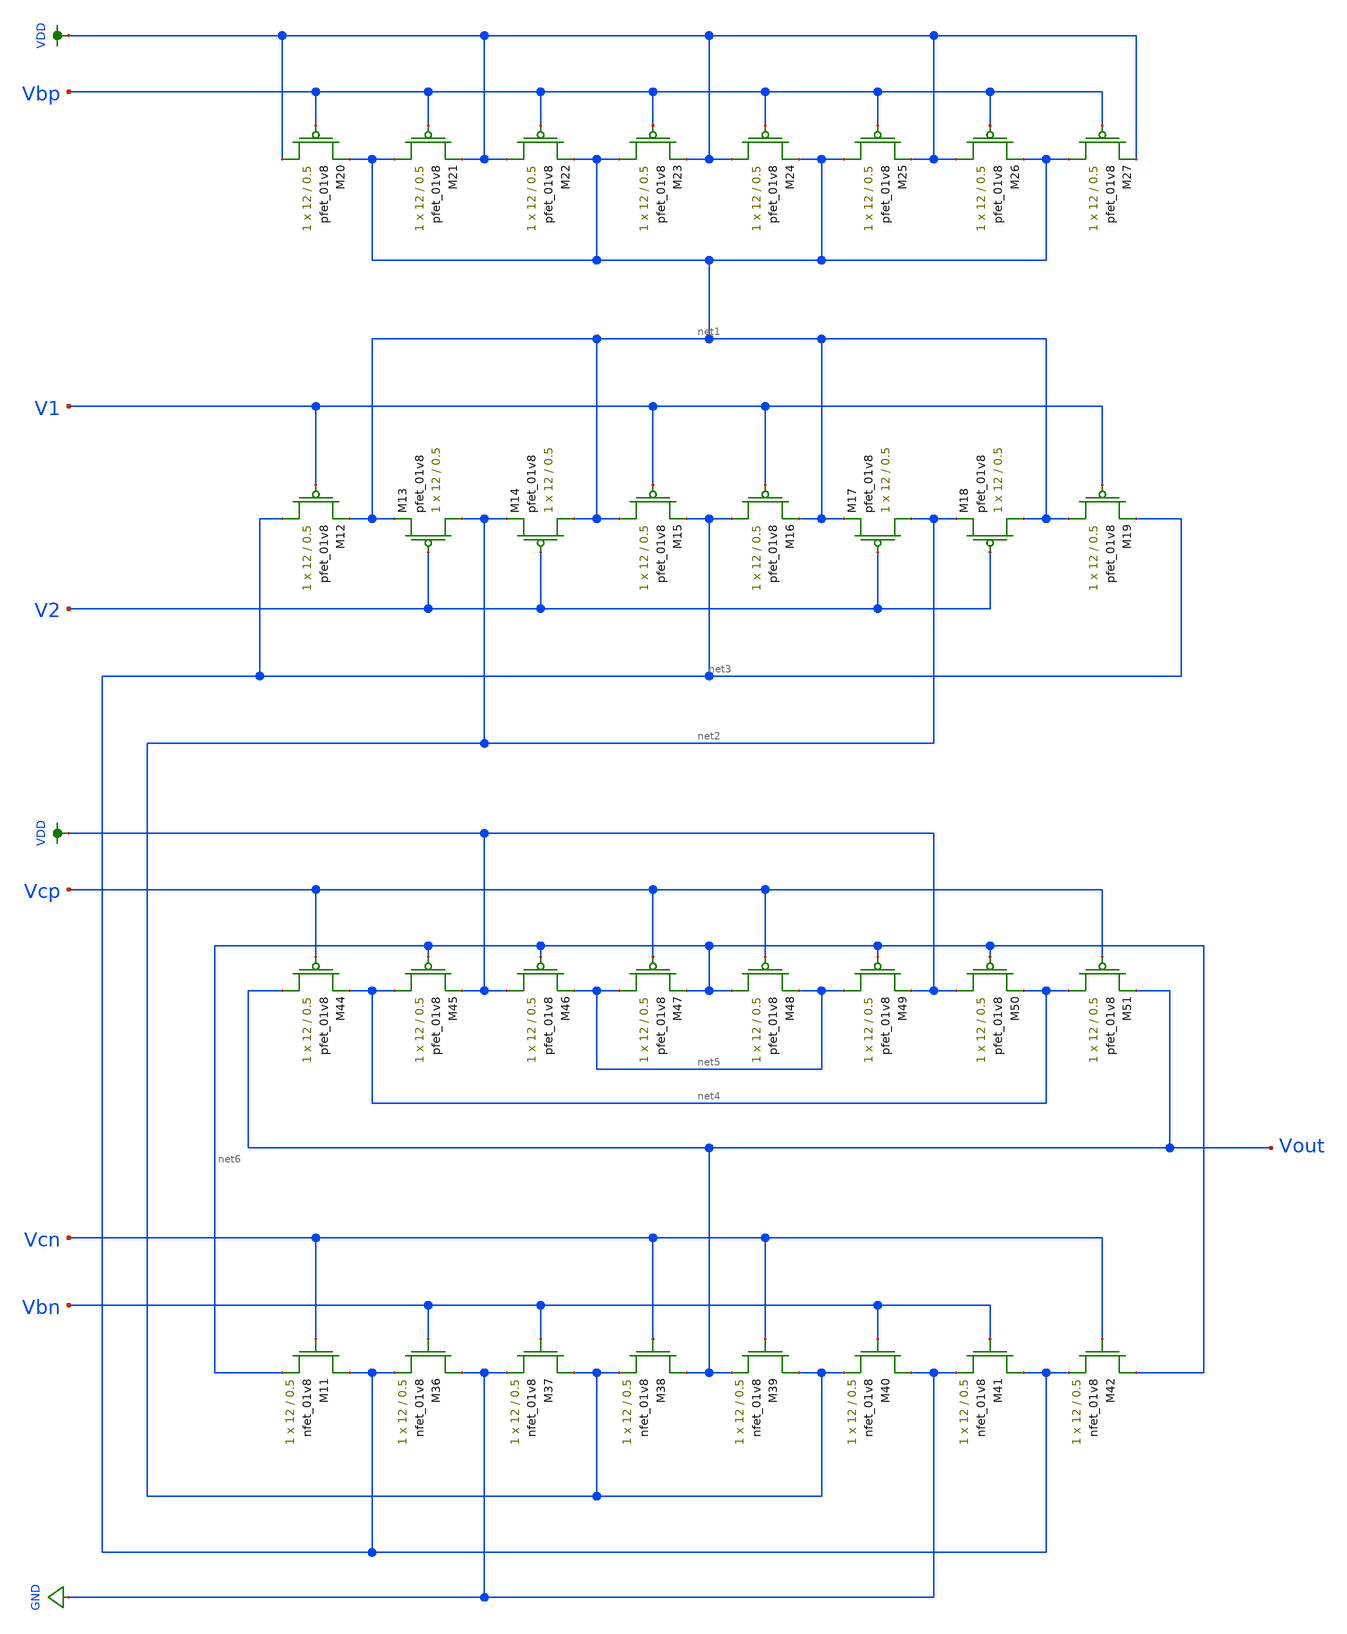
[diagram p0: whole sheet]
** sch_path: schematic/folded_cascode_differential_amplifier_LDS.sch
**.subckt folded_cascode_differential_amplifier_LDS
XM11 net3 Vcn net6 GND sky130_fd_pr__nfet_01v8 L=0.5 W=12 nf=1 ad='int((nf+1)/2) * W/nf * 0.29' as='int((nf+2)/2) * W/nf * 0.29'
+ pd='2*int((nf+1)/2) * (W/nf + 0.29)' ps='2*int((nf+2)/2) * (W/nf + 0.29)' nrd='0.29 / W' nrs='0.29 / W'
+ sa=0 sb=0 sd=0 mult=1 m=1
XM12 net3 V1 net1 VDD sky130_fd_pr__pfet_01v8 L=0.5 W=12 nf=1 ad='int((nf+1)/2) * W/nf * 0.29' as='int((nf+2)/2) * W/nf * 0.29'
+ pd='2*int((nf+1)/2) * (W/nf + 0.29)' ps='2*int((nf+2)/2) * (W/nf + 0.29)' nrd='0.29 / W' nrs='0.29 / W'
+ sa=0 sb=0 sd=0 mult=1 m=1
XM13 net2 V2 net1 VDD sky130_fd_pr__pfet_01v8 L=0.5 W=12 nf=1 ad='int((nf+1)/2) * W/nf * 0.29' as='int((nf+2)/2) * W/nf * 0.29'
+ pd='2*int((nf+1)/2) * (W/nf + 0.29)' ps='2*int((nf+2)/2) * (W/nf + 0.29)' nrd='0.29 / W' nrs='0.29 / W'
+ sa=0 sb=0 sd=0 mult=1 m=1
XM14 net1 V2 net2 VDD sky130_fd_pr__pfet_01v8 L=0.5 W=12 nf=1 ad='int((nf+1)/2) * W/nf * 0.29' as='int((nf+2)/2) * W/nf * 0.29'
+ pd='2*int((nf+1)/2) * (W/nf + 0.29)' ps='2*int((nf+2)/2) * (W/nf + 0.29)' nrd='0.29 / W' nrs='0.29 / W'
+ sa=0 sb=0 sd=0 mult=1 m=1
XM15 net1 V1 net3 VDD sky130_fd_pr__pfet_01v8 L=0.5 W=12 nf=1 ad='int((nf+1)/2) * W/nf * 0.29' as='int((nf+2)/2) * W/nf * 0.29'
+ pd='2*int((nf+1)/2) * (W/nf + 0.29)' ps='2*int((nf+2)/2) * (W/nf + 0.29)' nrd='0.29 / W' nrs='0.29 / W'
+ sa=0 sb=0 sd=0 mult=1 m=1
XM16 net3 V1 net1 VDD sky130_fd_pr__pfet_01v8 L=0.5 W=12 nf=1 ad='int((nf+1)/2) * W/nf * 0.29' as='int((nf+2)/2) * W/nf * 0.29'
+ pd='2*int((nf+1)/2) * (W/nf + 0.29)' ps='2*int((nf+2)/2) * (W/nf + 0.29)' nrd='0.29 / W' nrs='0.29 / W'
+ sa=0 sb=0 sd=0 mult=1 m=1
XM17 net2 V2 net1 VDD sky130_fd_pr__pfet_01v8 L=0.5 W=12 nf=1 ad='int((nf+1)/2) * W/nf * 0.29' as='int((nf+2)/2) * W/nf * 0.29'
+ pd='2*int((nf+1)/2) * (W/nf + 0.29)' ps='2*int((nf+2)/2) * (W/nf + 0.29)' nrd='0.29 / W' nrs='0.29 / W'
+ sa=0 sb=0 sd=0 mult=1 m=1
XM18 net1 V2 net2 VDD sky130_fd_pr__pfet_01v8 L=0.5 W=12 nf=1 ad='int((nf+1)/2) * W/nf * 0.29' as='int((nf+2)/2) * W/nf * 0.29'
+ pd='2*int((nf+1)/2) * (W/nf + 0.29)' ps='2*int((nf+2)/2) * (W/nf + 0.29)' nrd='0.29 / W' nrs='0.29 / W'
+ sa=0 sb=0 sd=0 mult=1 m=1
XM19 net1 V1 net3 VDD sky130_fd_pr__pfet_01v8 L=0.5 W=12 nf=1 ad='int((nf+1)/2) * W/nf * 0.29' as='int((nf+2)/2) * W/nf * 0.29'
+ pd='2*int((nf+1)/2) * (W/nf + 0.29)' ps='2*int((nf+2)/2) * (W/nf + 0.29)' nrd='0.29 / W' nrs='0.29 / W'
+ sa=0 sb=0 sd=0 mult=1 m=1
XM20 VDD Vbp net1 VDD sky130_fd_pr__pfet_01v8 L=0.5 W=12 nf=1 ad='int((nf+1)/2) * W/nf * 0.29' as='int((nf+2)/2) * W/nf * 0.29'
+ pd='2*int((nf+1)/2) * (W/nf + 0.29)' ps='2*int((nf+2)/2) * (W/nf + 0.29)' nrd='0.29 / W' nrs='0.29 / W'
+ sa=0 sb=0 sd=0 mult=1 m=1
XM21 net1 Vbp VDD VDD sky130_fd_pr__pfet_01v8 L=0.5 W=12 nf=1 ad='int((nf+1)/2) * W/nf * 0.29' as='int((nf+2)/2) * W/nf * 0.29'
+ pd='2*int((nf+1)/2) * (W/nf + 0.29)' ps='2*int((nf+2)/2) * (W/nf + 0.29)' nrd='0.29 / W' nrs='0.29 / W'
+ sa=0 sb=0 sd=0 mult=1 m=1
XM22 VDD Vbp net1 VDD sky130_fd_pr__pfet_01v8 L=0.5 W=12 nf=1 ad='int((nf+1)/2) * W/nf * 0.29' as='int((nf+2)/2) * W/nf * 0.29'
+ pd='2*int((nf+1)/2) * (W/nf + 0.29)' ps='2*int((nf+2)/2) * (W/nf + 0.29)' nrd='0.29 / W' nrs='0.29 / W'
+ sa=0 sb=0 sd=0 mult=1 m=1
XM23 net1 Vbp VDD VDD sky130_fd_pr__pfet_01v8 L=0.5 W=12 nf=1 ad='int((nf+1)/2) * W/nf * 0.29' as='int((nf+2)/2) * W/nf * 0.29'
+ pd='2*int((nf+1)/2) * (W/nf + 0.29)' ps='2*int((nf+2)/2) * (W/nf + 0.29)' nrd='0.29 / W' nrs='0.29 / W'
+ sa=0 sb=0 sd=0 mult=1 m=1
XM24 VDD Vbp net1 VDD sky130_fd_pr__pfet_01v8 L=0.5 W=12 nf=1 ad='int((nf+1)/2) * W/nf * 0.29' as='int((nf+2)/2) * W/nf * 0.29'
+ pd='2*int((nf+1)/2) * (W/nf + 0.29)' ps='2*int((nf+2)/2) * (W/nf + 0.29)' nrd='0.29 / W' nrs='0.29 / W'
+ sa=0 sb=0 sd=0 mult=1 m=1
XM25 net1 Vbp VDD VDD sky130_fd_pr__pfet_01v8 L=0.5 W=12 nf=1 ad='int((nf+1)/2) * W/nf * 0.29' as='int((nf+2)/2) * W/nf * 0.29'
+ pd='2*int((nf+1)/2) * (W/nf + 0.29)' ps='2*int((nf+2)/2) * (W/nf + 0.29)' nrd='0.29 / W' nrs='0.29 / W'
+ sa=0 sb=0 sd=0 mult=1 m=1
XM26 VDD Vbp net1 VDD sky130_fd_pr__pfet_01v8 L=0.5 W=12 nf=1 ad='int((nf+1)/2) * W/nf * 0.29' as='int((nf+2)/2) * W/nf * 0.29'
+ pd='2*int((nf+1)/2) * (W/nf + 0.29)' ps='2*int((nf+2)/2) * (W/nf + 0.29)' nrd='0.29 / W' nrs='0.29 / W'
+ sa=0 sb=0 sd=0 mult=1 m=1
XM27 net1 Vbp VDD VDD sky130_fd_pr__pfet_01v8 L=0.5 W=12 nf=1 ad='int((nf+1)/2) * W/nf * 0.29' as='int((nf+2)/2) * W/nf * 0.29'
+ pd='2*int((nf+1)/2) * (W/nf + 0.29)' ps='2*int((nf+2)/2) * (W/nf + 0.29)' nrd='0.29 / W' nrs='0.29 / W'
+ sa=0 sb=0 sd=0 mult=1 m=1
XM36 GND Vbn net3 GND sky130_fd_pr__nfet_01v8 L=0.5 W=12 nf=1 ad='int((nf+1)/2) * W/nf * 0.29' as='int((nf+2)/2) * W/nf * 0.29'
+ pd='2*int((nf+1)/2) * (W/nf + 0.29)' ps='2*int((nf+2)/2) * (W/nf + 0.29)' nrd='0.29 / W' nrs='0.29 / W'
+ sa=0 sb=0 sd=0 mult=1 m=1
XM37 net2 Vbn GND GND sky130_fd_pr__nfet_01v8 L=0.5 W=12 nf=1 ad='int((nf+1)/2) * W/nf * 0.29' as='int((nf+2)/2) * W/nf * 0.29'
+ pd='2*int((nf+1)/2) * (W/nf + 0.29)' ps='2*int((nf+2)/2) * (W/nf + 0.29)' nrd='0.29 / W' nrs='0.29 / W'
+ sa=0 sb=0 sd=0 mult=1 m=1
XM38 Vout Vcn net2 GND sky130_fd_pr__nfet_01v8 L=0.5 W=12 nf=1 ad='int((nf+1)/2) * W/nf * 0.29' as='int((nf+2)/2) * W/nf * 0.29'
+ pd='2*int((nf+1)/2) * (W/nf + 0.29)' ps='2*int((nf+2)/2) * (W/nf + 0.29)' nrd='0.29 / W' nrs='0.29 / W'
+ sa=0 sb=0 sd=0 mult=1 m=1
XM39 net2 Vcn Vout GND sky130_fd_pr__nfet_01v8 L=0.5 W=12 nf=1 ad='int((nf+1)/2) * W/nf * 0.29' as='int((nf+2)/2) * W/nf * 0.29'
+ pd='2*int((nf+1)/2) * (W/nf + 0.29)' ps='2*int((nf+2)/2) * (W/nf + 0.29)' nrd='0.29 / W' nrs='0.29 / W'
+ sa=0 sb=0 sd=0 mult=1 m=1
XM40 GND Vbn net2 GND sky130_fd_pr__nfet_01v8 L=0.5 W=12 nf=1 ad='int((nf+1)/2) * W/nf * 0.29' as='int((nf+2)/2) * W/nf * 0.29'
+ pd='2*int((nf+1)/2) * (W/nf + 0.29)' ps='2*int((nf+2)/2) * (W/nf + 0.29)' nrd='0.29 / W' nrs='0.29 / W'
+ sa=0 sb=0 sd=0 mult=1 m=1
XM41 net3 Vbn GND GND sky130_fd_pr__nfet_01v8 L=0.5 W=12 nf=1 ad='int((nf+1)/2) * W/nf * 0.29' as='int((nf+2)/2) * W/nf * 0.29'
+ pd='2*int((nf+1)/2) * (W/nf + 0.29)' ps='2*int((nf+2)/2) * (W/nf + 0.29)' nrd='0.29 / W' nrs='0.29 / W'
+ sa=0 sb=0 sd=0 mult=1 m=1
XM42 net6 Vcn net3 GND sky130_fd_pr__nfet_01v8 L=0.5 W=12 nf=1 ad='int((nf+1)/2) * W/nf * 0.29' as='int((nf+2)/2) * W/nf * 0.29'
+ pd='2*int((nf+1)/2) * (W/nf + 0.29)' ps='2*int((nf+2)/2) * (W/nf + 0.29)' nrd='0.29 / W' nrs='0.29 / W'
+ sa=0 sb=0 sd=0 mult=1 m=1
XM44 Vout Vcp net4 VDD sky130_fd_pr__pfet_01v8 L=0.5 W=12 nf=1 ad='int((nf+1)/2) * W/nf * 0.29' as='int((nf+2)/2) * W/nf * 0.29'
+ pd='2*int((nf+1)/2) * (W/nf + 0.29)' ps='2*int((nf+2)/2) * (W/nf + 0.29)' nrd='0.29 / W' nrs='0.29 / W'
+ sa=0 sb=0 sd=0 mult=1 m=1
XM45 net4 net6 VDD VDD sky130_fd_pr__pfet_01v8 L=0.5 W=12 nf=1 ad='int((nf+1)/2) * W/nf * 0.29' as='int((nf+2)/2) * W/nf * 0.29'
+ pd='2*int((nf+1)/2) * (W/nf + 0.29)' ps='2*int((nf+2)/2) * (W/nf + 0.29)' nrd='0.29 / W' nrs='0.29 / W'
+ sa=0 sb=0 sd=0 mult=1 m=1
XM46 VDD net6 net5 VDD sky130_fd_pr__pfet_01v8 L=0.5 W=12 nf=1 ad='int((nf+1)/2) * W/nf * 0.29' as='int((nf+2)/2) * W/nf * 0.29'
+ pd='2*int((nf+1)/2) * (W/nf + 0.29)' ps='2*int((nf+2)/2) * (W/nf + 0.29)' nrd='0.29 / W' nrs='0.29 / W'
+ sa=0 sb=0 sd=0 mult=1 m=1
XM47 net5 Vcp net6 VDD sky130_fd_pr__pfet_01v8 L=0.5 W=12 nf=1 ad='int((nf+1)/2) * W/nf * 0.29' as='int((nf+2)/2) * W/nf * 0.29'
+ pd='2*int((nf+1)/2) * (W/nf + 0.29)' ps='2*int((nf+2)/2) * (W/nf + 0.29)' nrd='0.29 / W' nrs='0.29 / W'
+ sa=0 sb=0 sd=0 mult=1 m=1
XM48 net6 Vcp net5 VDD sky130_fd_pr__pfet_01v8 L=0.5 W=12 nf=1 ad='int((nf+1)/2) * W/nf * 0.29' as='int((nf+2)/2) * W/nf * 0.29'
+ pd='2*int((nf+1)/2) * (W/nf + 0.29)' ps='2*int((nf+2)/2) * (W/nf + 0.29)' nrd='0.29 / W' nrs='0.29 / W'
+ sa=0 sb=0 sd=0 mult=1 m=1
XM49 net5 net6 VDD VDD sky130_fd_pr__pfet_01v8 L=0.5 W=12 nf=1 ad='int((nf+1)/2) * W/nf * 0.29' as='int((nf+2)/2) * W/nf * 0.29'
+ pd='2*int((nf+1)/2) * (W/nf + 0.29)' ps='2*int((nf+2)/2) * (W/nf + 0.29)' nrd='0.29 / W' nrs='0.29 / W'
+ sa=0 sb=0 sd=0 mult=1 m=1
XM50 VDD net6 net4 VDD sky130_fd_pr__pfet_01v8 L=0.5 W=12 nf=1 ad='int((nf+1)/2) * W/nf * 0.29' as='int((nf+2)/2) * W/nf * 0.29'
+ pd='2*int((nf+1)/2) * (W/nf + 0.29)' ps='2*int((nf+2)/2) * (W/nf + 0.29)' nrd='0.29 / W' nrs='0.29 / W'
+ sa=0 sb=0 sd=0 mult=1 m=1
XM51 net4 Vcp Vout VDD sky130_fd_pr__pfet_01v8 L=0.5 W=12 nf=1 ad='int((nf+1)/2) * W/nf * 0.29' as='int((nf+2)/2) * W/nf * 0.29'
+ pd='2*int((nf+1)/2) * (W/nf + 0.29)' ps='2*int((nf+2)/2) * (W/nf + 0.29)' nrd='0.29 / W' nrs='0.29 / W'
+ sa=0 sb=0 sd=0 mult=1 m=1
**.ends
.GLOBAL VDD
.GLOBAL GND
.end
